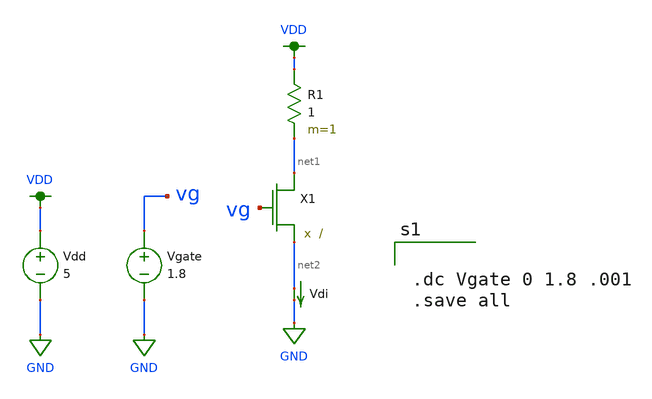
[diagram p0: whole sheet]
** sch_path: schematics/power_nfet_test.sch
**.subckt power_nfet_test
Vdd VDD GND 5
Vdi net2 GND 0
.save i(vdi)
X1 net1 vg net2 power_nfet
Vgate vg GND 1.8
R1 VDD net1 1 m=1
**** begin user architecture code


.dc Vgate 0 1.8 .001
.save all



*SRC=DMN2009LSS;DI_DMN2009LSS;MOSFETs N;Enh;20.0V 12.0A 8.00mohms  Diodes Inc. MOSFET
*SYM=POWMOSN
.SUBCKT power_nfet 10 20 30
*     TERMINALS:  D  G  S
M1   1  2  3  3  DMOS L=1U W=1U
RD  10  1  2.80m
RS  40  3  1.20m
RG  20  2  12.5
CGS  2  3  2.46n
EGD 12  0  2  1  1
VFB 14  0  0
FFB  2  1  VFB  1
CGD 13 14  663p
R1  13  0  1.00
D1  12 13  DLIM
DDG 15 14  DCGD
R2  12 15  1.00
D2  15  0  DLIM
DSD  3 10  DSUB
LS  30 40  7.50n
.model DMOS NMOS(LEVEL=3 VMAX=41.7k THETA=60.0m  ETA=2.00m VTO=1 KP=274
.model DCGD D (CJO=663p VJ=0.600 M=0.680
.model DSUB D (IS=49.8n N=1.50 RS=37.5m BV=20.0  CJO=1.28n VJ=0.800 M=0.420 TT=297n
.model DLIM D (IS=100U)
.ends

**** end user architecture code
**.ends
.GLOBAL VDD
.GLOBAL GND
.end
